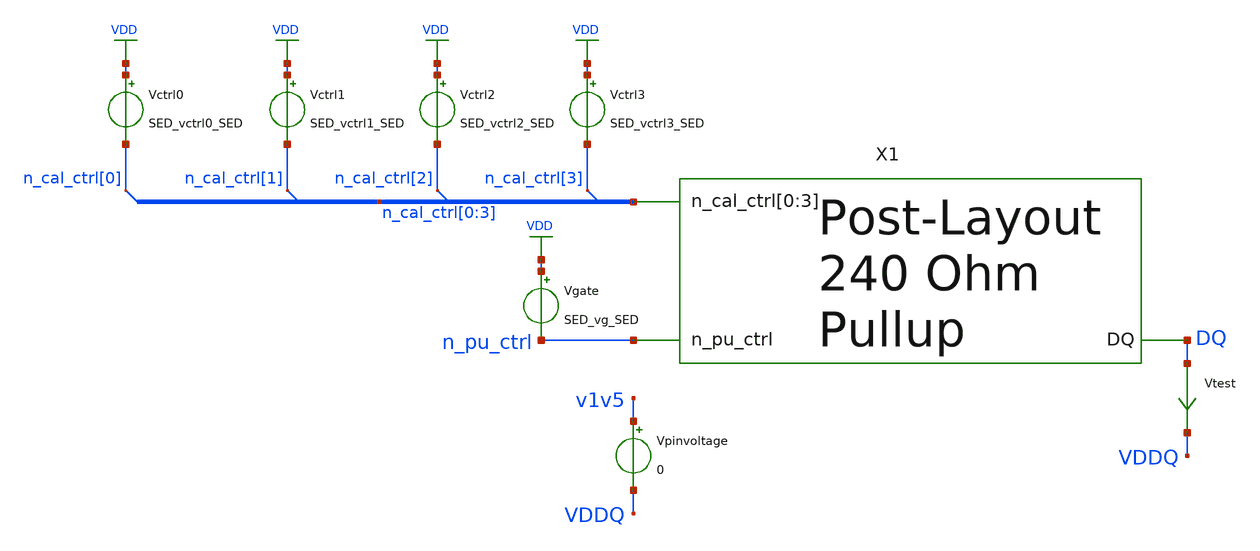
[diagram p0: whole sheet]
** sch_path: schem/post_layout_p-leg_tb.sch
* Copyright 2021 Stefan Frederik Schippers
* Licensed under the Apache License, Version 2.0 (the "License");
* you may not use this file except in compliance with the License.
* You may obtain a copy of the License at
* https://www.apache.org/licenses/LICENSE-2.0
* Unless required by applicable law or agreed to in writing, software
* distributed under the License is distributed on an "AS IS" BASIS,
* WITHOUT WARRANTIES OR CONDITIONS OF ANY KIND, either express or implied.
* See the License for the specific language governing permissions and
* limitations under the License.
**.subckt post_layout_p-leg_tb
Vctrl0 VDD n_cal_ctrl[0] SED_vctrl0_SED
Vctrl1 VDD n_cal_ctrl[1] SED_vctrl1_SED
Vctrl2 VDD n_cal_ctrl[2] SED_vctrl2_SED
Vctrl3 VDD n_cal_ctrl[3] SED_vctrl3_SED
Vgate VDD n_pu_ctrl SED_vg_SED
Vtest DQ VDDQ 0
.save i(vtest)
Vpinvoltage v1v5 VDDQ 0
X1 DQ VDD n_cal_ctrl[0] n_cal_ctrl[1] n_cal_ctrl[2] n_cal_ctrl[3] n_pu_ctrl p-leg_flat
**** begin user architecture code
 ** Local library links to pdk
.lib ./sky130/libs/SED_process_SED_lib.spice SED_process_SED
.include ./layout/pex_p-leg.spice

**** end user architecture code
**.ends
.GLOBAL VDD
**** begin user architecture code



* power voltage
vvdd VDD 0 SED_vdd_SED
vv1v5 v1v5 0 1.5

.control
save all
set temp=SED_temp_SED

* RUN SIMULATION
dc Vpinvoltage 0.3 1.2 0.05
* OUTPUT
print (SED_vdd_SED-vddq)/i(vtest)
wrdata out/SED_plotName_SED/SED_plotName_SED.txt (SED_vdd_SED-vddq)/i(vtest)
set hcopydevtype = svg
hardcopy ./out/SED_plotName_SED/SED_plotName_SED.svg (SED_vdd_SED-vddq)/I(vtest) vs vddq title 'Resistance vs pin voltage'

.endc


**** end user architecture code
.end
